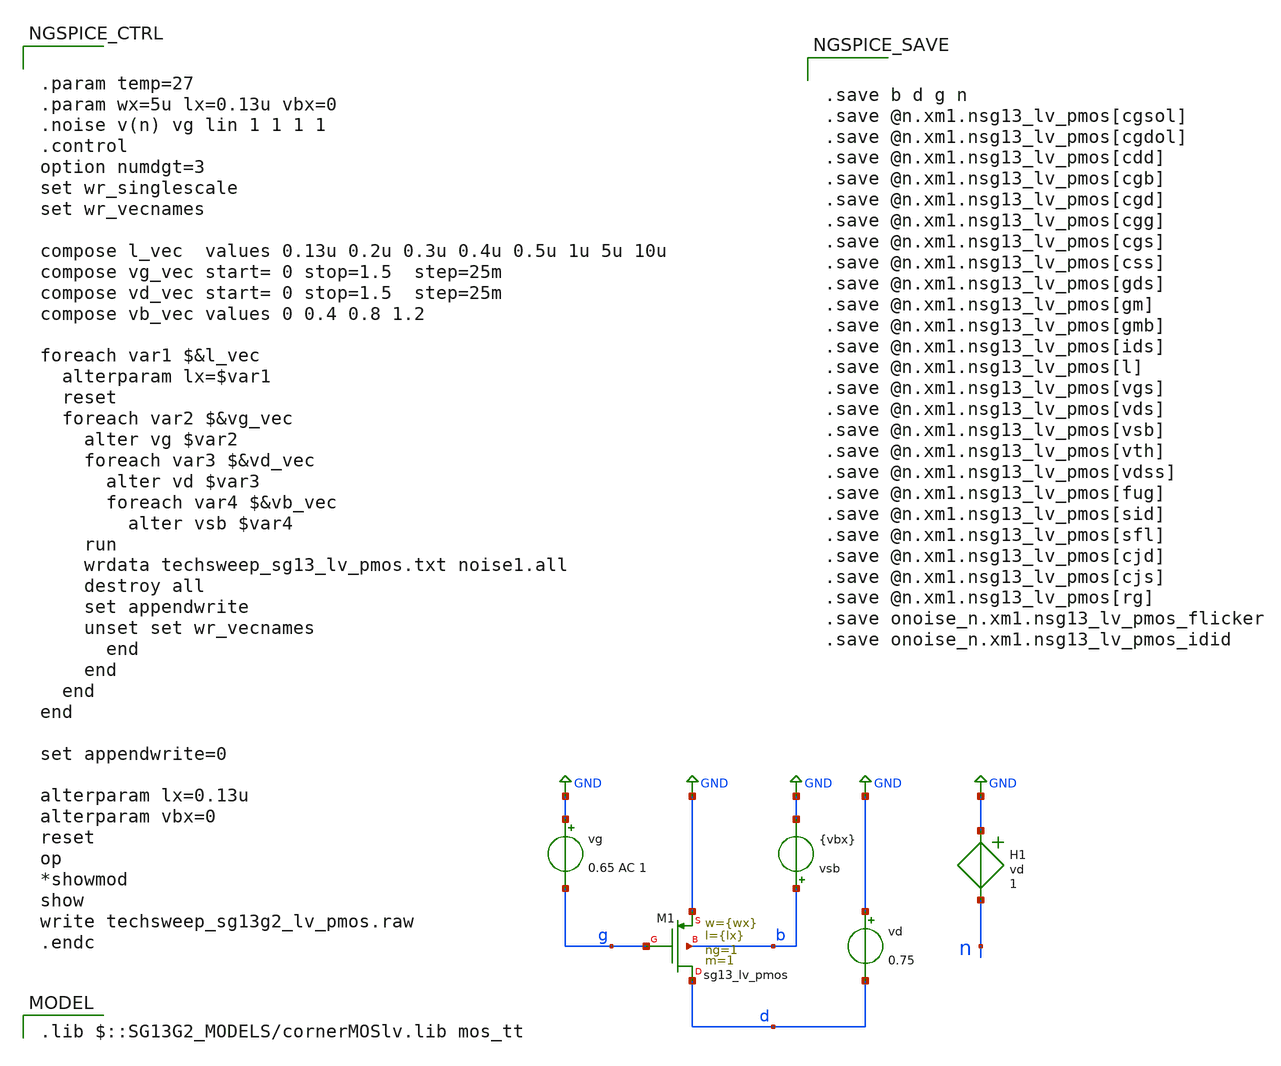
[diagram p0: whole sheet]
** sch_path: xschem/techsweep_sg13g2_lv_pmos.sch
* (c) 2024 Harald Pretl (adapted from Boris Murmann)
**.subckt techsweep_sg13g2_lv_pmos
XM1 d g GND b sg13_lv_pmos w={wx} l={lx} ng=1 m=1 mm_ok=1
vd GND d 0.75
vsb b GND {vbx}
vg GND g 0.65 AC 1
H1 GND n vd 1
**** begin user architecture code
 .lib $::SG13G2_MODELS/cornerMOSlv.lib mos_tt



.save b d g n
.save @n.xm1.nsg13_lv_pmos[cgsol]
.save @n.xm1.nsg13_lv_pmos[cgdol]
.save @n.xm1.nsg13_lv_pmos[cdd]
.save @n.xm1.nsg13_lv_pmos[cgb]
.save @n.xm1.nsg13_lv_pmos[cgd]
.save @n.xm1.nsg13_lv_pmos[cgg]
.save @n.xm1.nsg13_lv_pmos[cgs]
.save @n.xm1.nsg13_lv_pmos[css]
.save @n.xm1.nsg13_lv_pmos[gds]
.save @n.xm1.nsg13_lv_pmos[gm]
.save @n.xm1.nsg13_lv_pmos[gmb]
.save @n.xm1.nsg13_lv_pmos[ids]
.save @n.xm1.nsg13_lv_pmos[l]
.save @n.xm1.nsg13_lv_pmos[vgs]
.save @n.xm1.nsg13_lv_pmos[vds]
.save @n.xm1.nsg13_lv_pmos[vsb]
.save @n.xm1.nsg13_lv_pmos[vth]
.save @n.xm1.nsg13_lv_pmos[vdss]
.save @n.xm1.nsg13_lv_pmos[fug]
.save @n.xm1.nsg13_lv_pmos[sid]
.save @n.xm1.nsg13_lv_pmos[sfl]
.save @n.xm1.nsg13_lv_pmos[cjd]
.save @n.xm1.nsg13_lv_pmos[cjs]
.save @n.xm1.nsg13_lv_pmos[rg]
.save onoise_n.xm1.nsg13_lv_pmos_flicker
.save onoise_n.xm1.nsg13_lv_pmos_idid




.param temp=27
.param wx=5u lx=0.13u vbx=0
.noise v(n) vg lin 1 1 1 1
.control
option numdgt=3
set wr_singlescale
set wr_vecnames

compose l_vec  values 0.13u 0.2u 0.3u 0.4u 0.5u 1u 5u 10u
compose vg_vec start= 0 stop=1.5  step=25m
compose vd_vec start= 0 stop=1.5  step=25m
compose vb_vec values 0 0.4 0.8 1.2

foreach var1 $&l_vec
  alterparam lx=$var1
  reset
  foreach var2 $&vg_vec
    alter vg $var2
    foreach var3 $&vd_vec
      alter vd $var3
      foreach var4 $&vb_vec
        alter vsb $var4
	run
	wrdata techsweep_sg13_lv_pmos.txt noise1.all
	destroy all
	set appendwrite
	unset set wr_vecnames
      end
    end
  end
end

set appendwrite=0

alterparam lx=0.13u
alterparam vbx=0
reset
op
*showmod
show
write techsweep_sg13g2_lv_pmos.raw
.endc


**** end user architecture code
**.ends
.GLOBAL GND
.end
